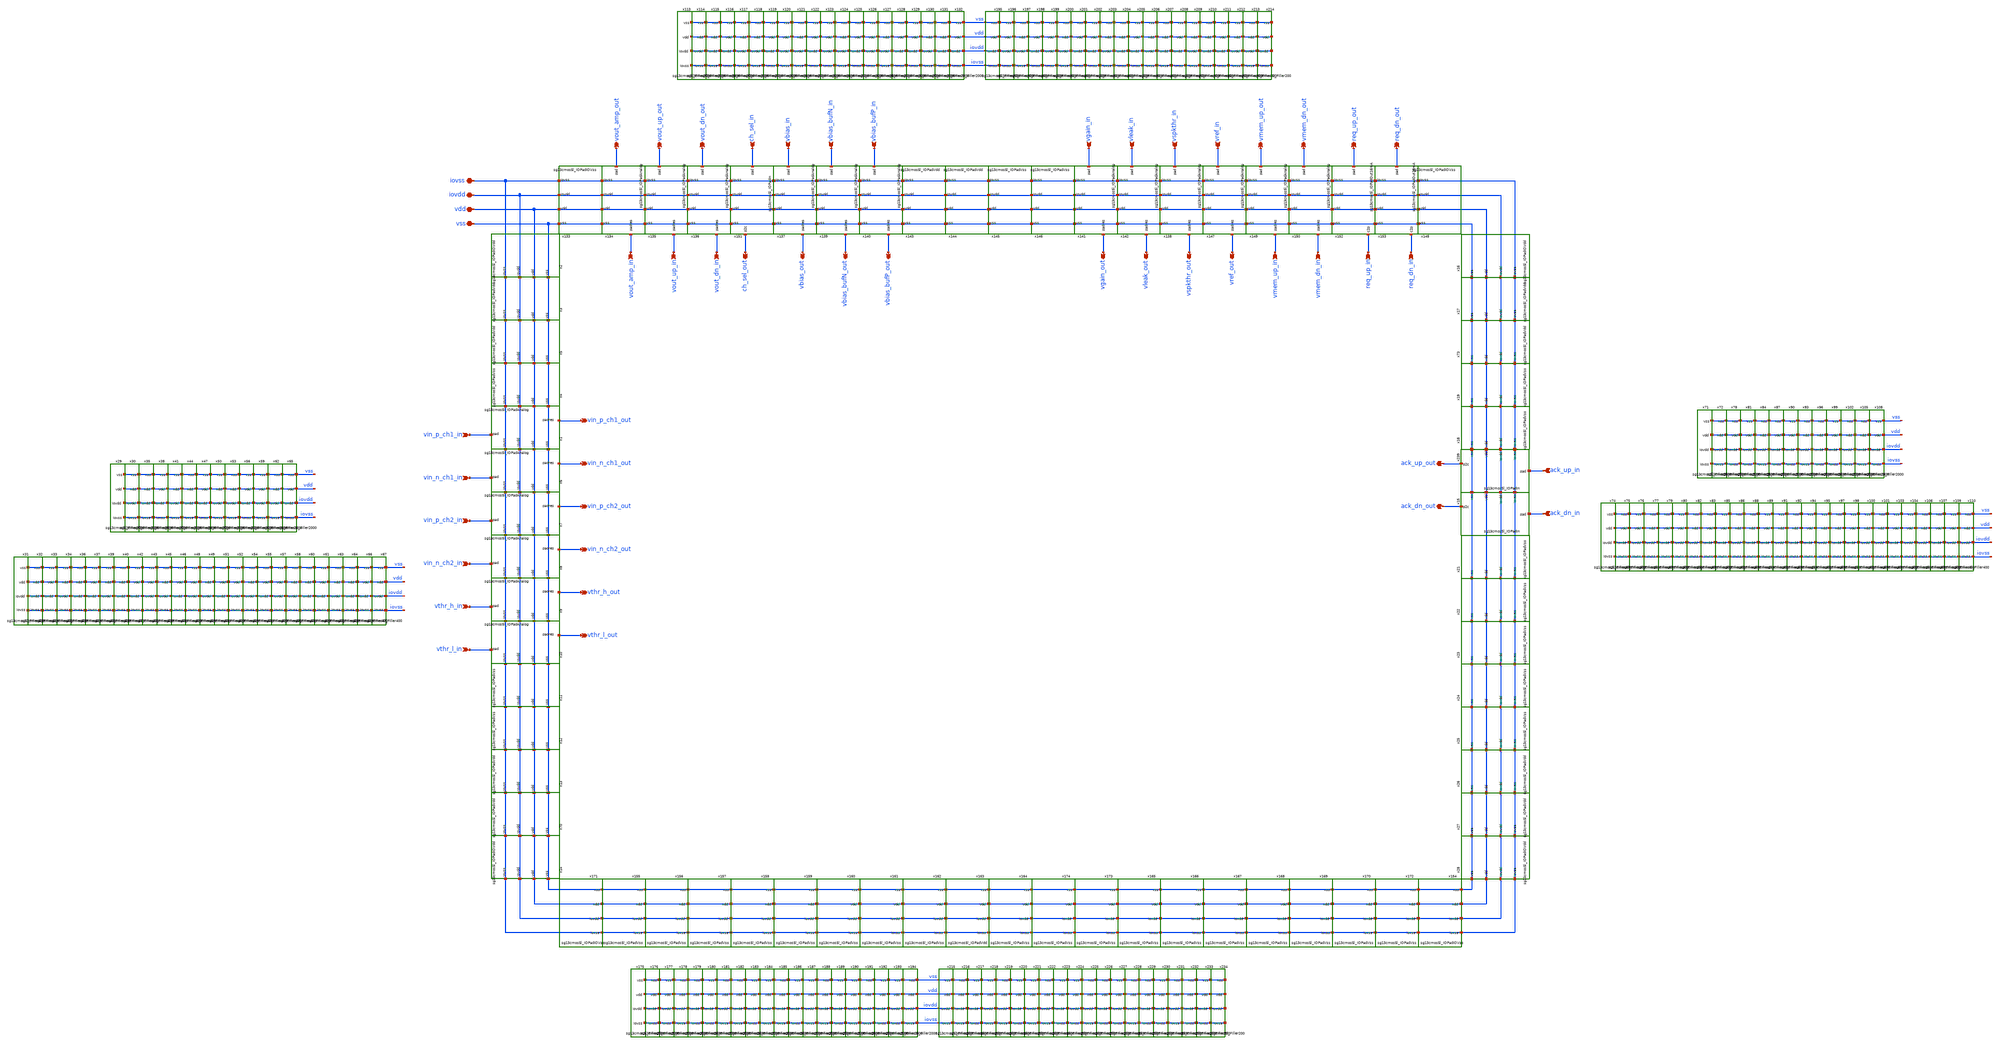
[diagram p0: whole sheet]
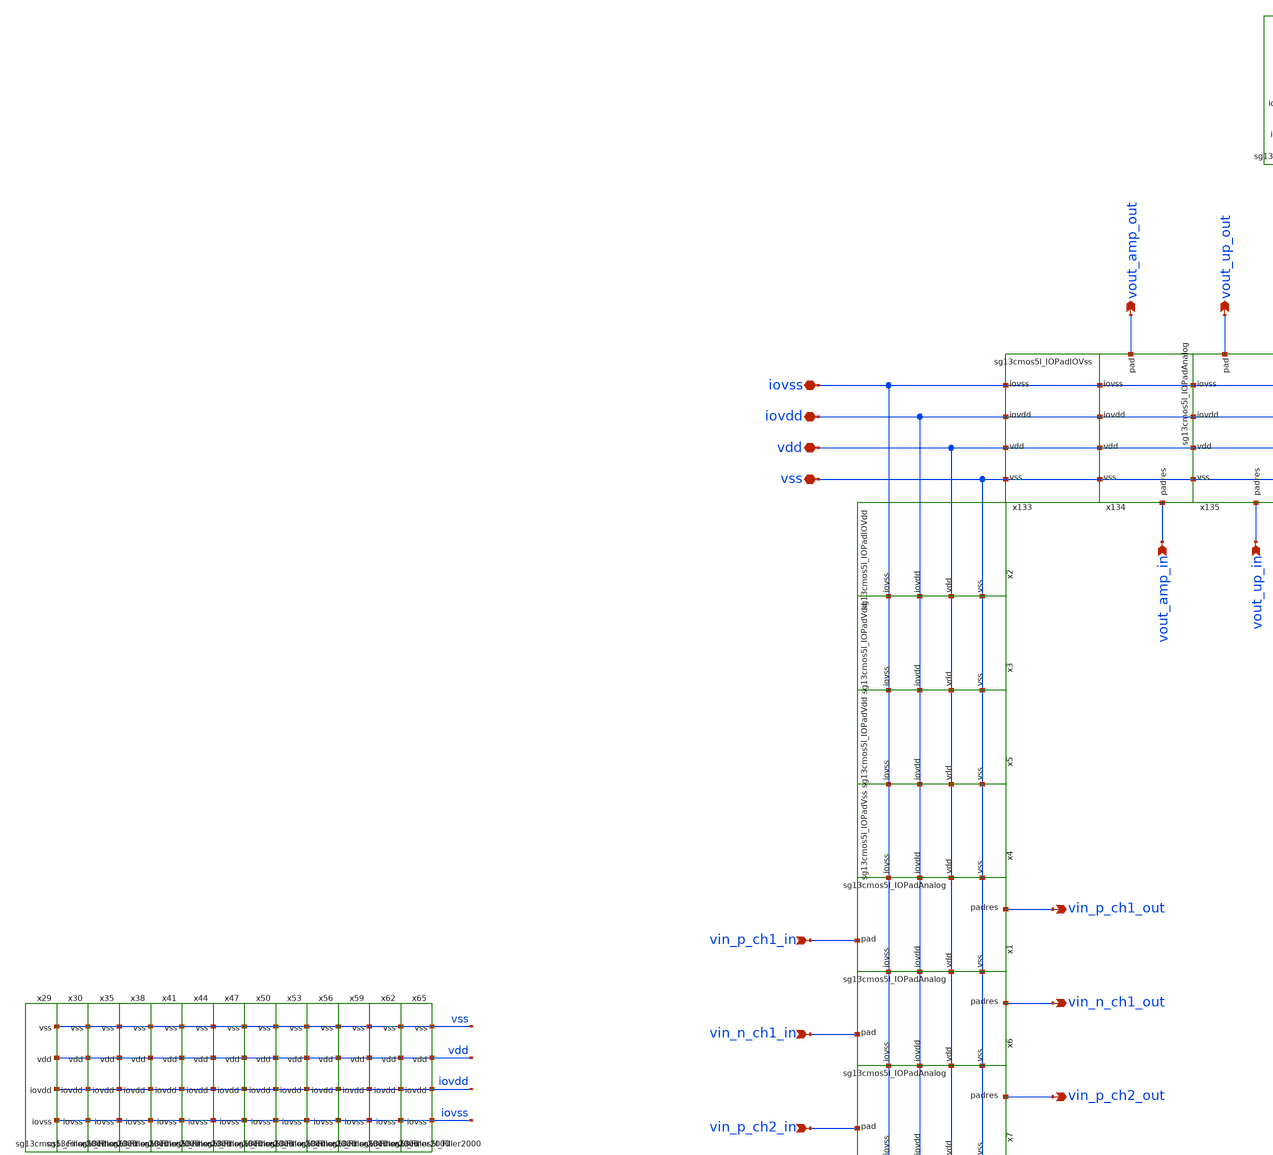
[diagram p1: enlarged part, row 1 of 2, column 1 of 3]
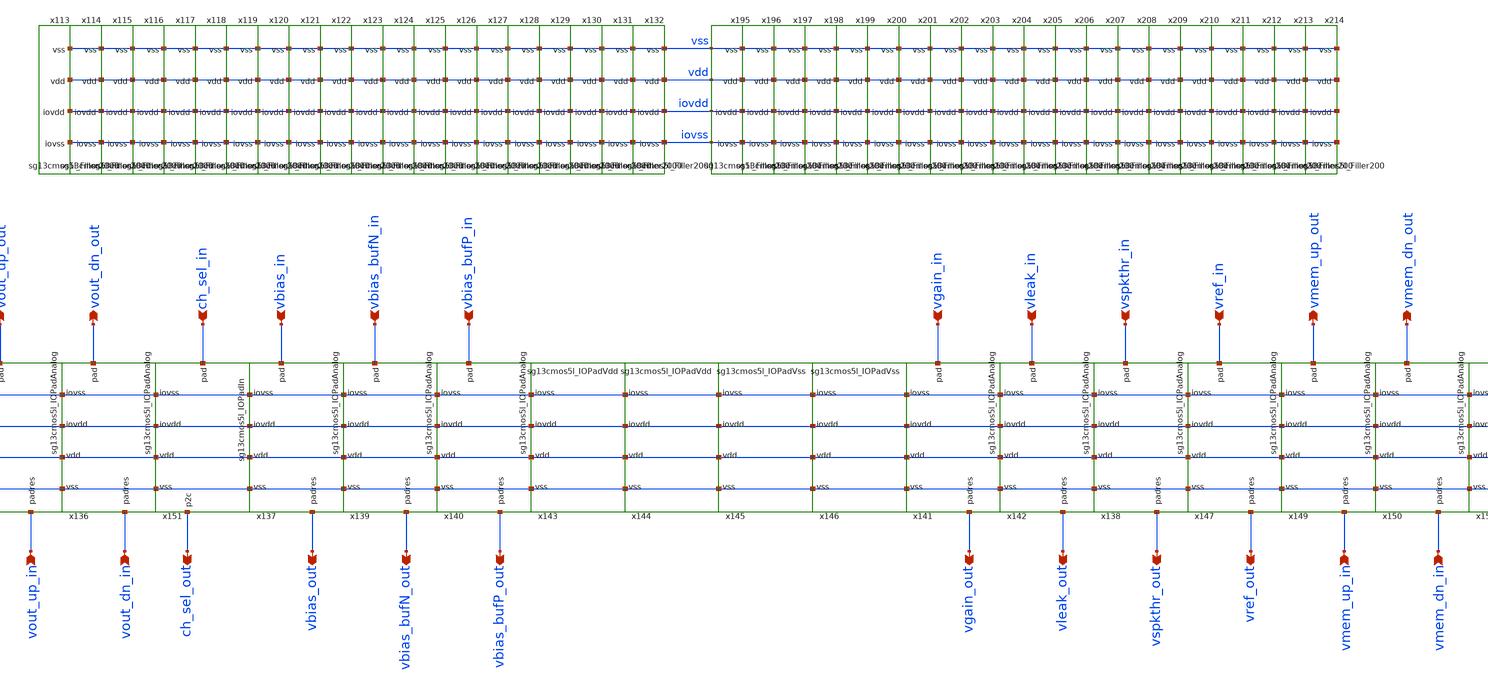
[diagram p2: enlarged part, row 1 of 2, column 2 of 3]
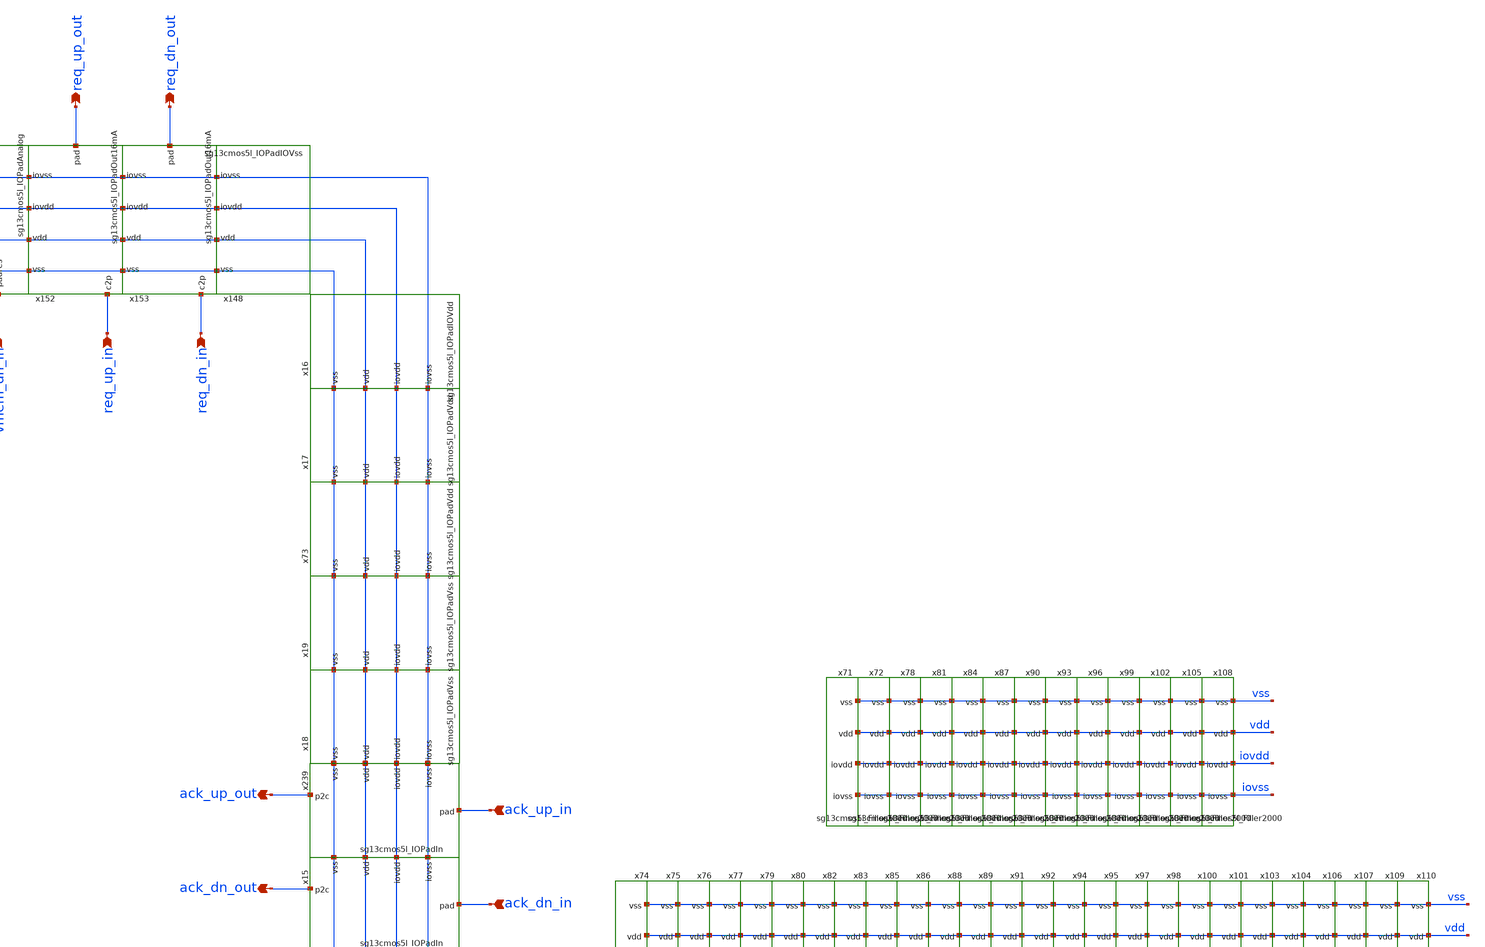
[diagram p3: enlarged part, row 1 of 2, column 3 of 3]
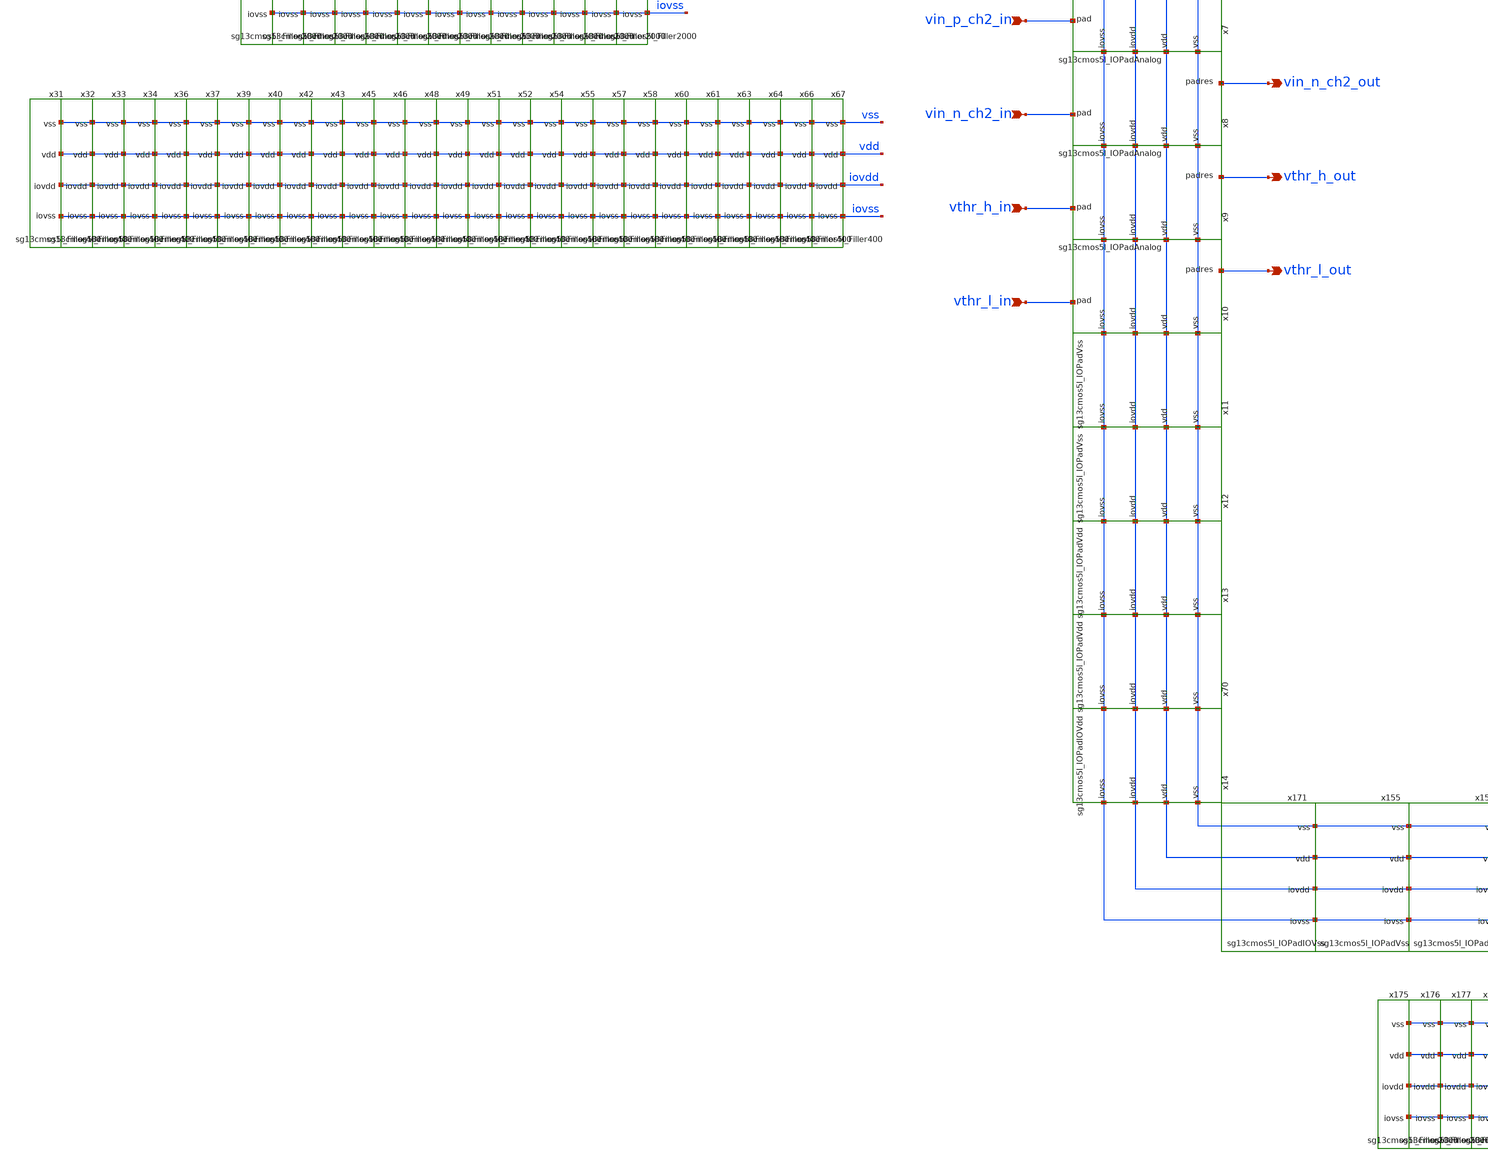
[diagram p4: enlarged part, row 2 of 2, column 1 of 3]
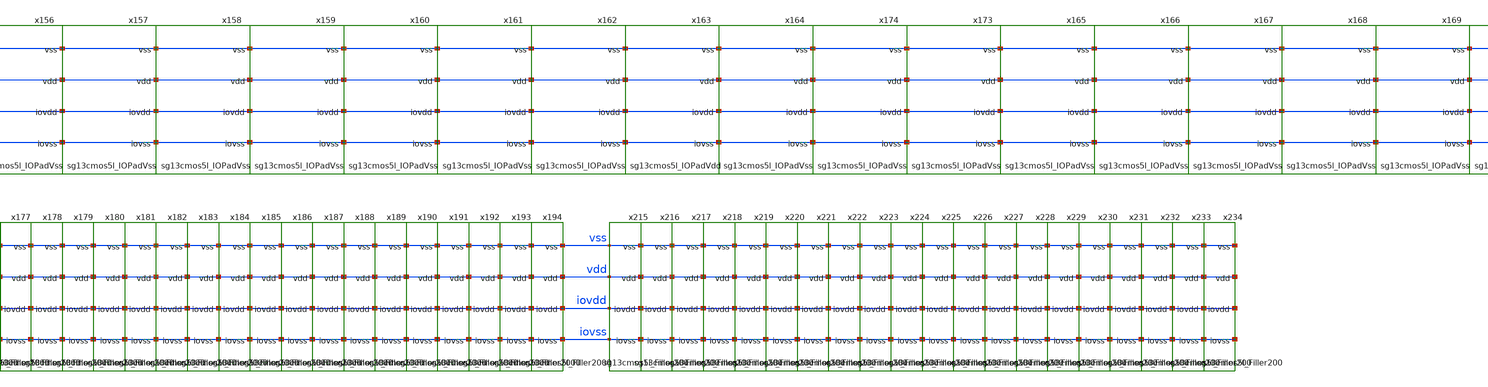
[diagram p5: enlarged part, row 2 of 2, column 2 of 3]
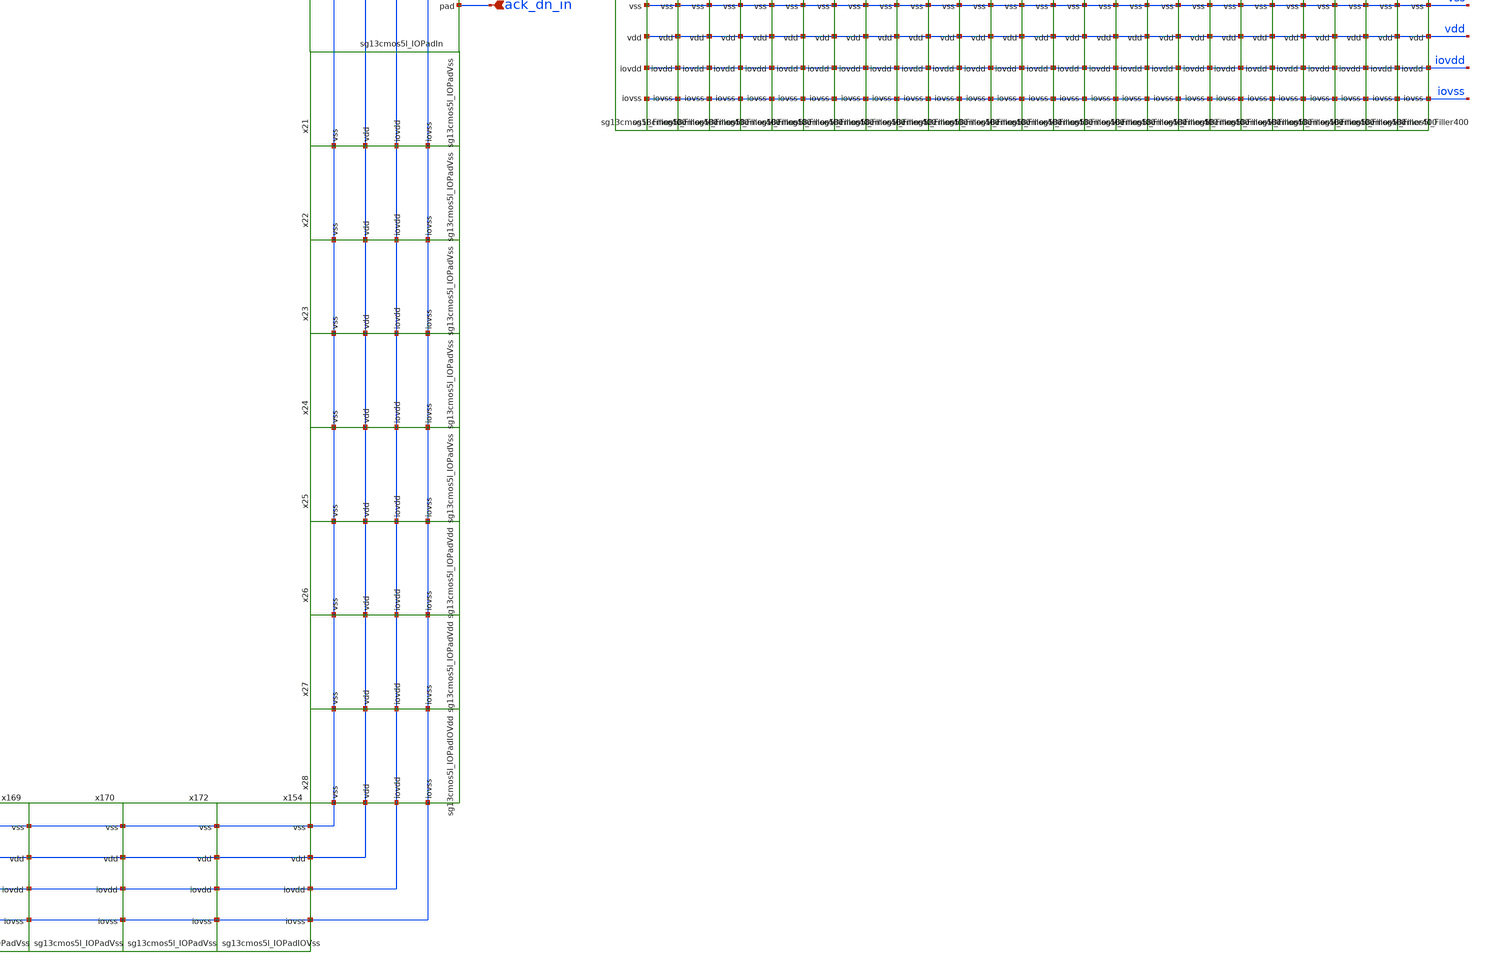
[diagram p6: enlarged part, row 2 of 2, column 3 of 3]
** sch_path: v2_feature_extr/padframe_old.sch
**.subckt padframe_old iovss iovdd vdd vss vin_p_ch1_in vin_n_ch1_in vin_p_ch2_in vin_n_ch2_in
*+ vin_p_ch1_out vin_n_ch1_out vin_p_ch2_out vin_n_ch2_out vthr_h_in vthr_l_in vthr_h_out vthr_l_out vout_amp_in
*+ vout_up_in vout_dn_in vout_amp_out vout_up_out vout_dn_out ch_sel_in ch_sel_out vbias_in vbias_out
*+ vbias_bufN_in vbias_bufN_out vbias_bufP_in vbias_bufP_out vgain_in vleak_in vspkthr_in vref_in vgain_out
*+ vleak_out vspkthr_out vref_out vmem_up_in vmem_dn_in req_up_in req_dn_in vmem_up_out vmem_dn_out req_up_out
*+ req_dn_out ack_up_in ack_up_out ack_dn_in ack_dn_out
*.iopin iovss
*.iopin iovdd
*.iopin vdd
*.iopin vss
*.ipin vin_p_ch1_in
*.ipin vin_n_ch1_in
*.ipin vin_p_ch2_in
*.ipin vin_n_ch2_in
*.opin vin_p_ch1_out
*.opin vin_n_ch1_out
*.opin vin_p_ch2_out
*.opin vin_n_ch2_out
*.ipin vthr_h_in
*.ipin vthr_l_in
*.opin vthr_h_out
*.opin vthr_l_out
*.ipin vout_amp_in
*.ipin vout_up_in
*.ipin vout_dn_in
*.opin vout_amp_out
*.opin vout_up_out
*.opin vout_dn_out
*.ipin ch_sel_in
*.opin ch_sel_out
*.ipin vbias_in
*.opin vbias_out
*.ipin vbias_bufN_in
*.opin vbias_bufN_out
*.ipin vbias_bufP_in
*.opin vbias_bufP_out
*.ipin vgain_in
*.ipin vleak_in
*.ipin vspkthr_in
*.ipin vref_in
*.opin vgain_out
*.opin vleak_out
*.opin vspkthr_out
*.opin vref_out
*.ipin vmem_up_in
*.ipin vmem_dn_in
*.ipin req_up_in
*.ipin req_dn_in
*.opin vmem_up_out
*.opin vmem_dn_out
*.opin req_up_out
*.opin req_dn_out
*.ipin ack_up_in
*.opin ack_up_out
*.ipin ack_dn_in
*.opin ack_dn_out
x1 iovdd iovss vin_p_ch1_in vin_p_ch1_out vdd vss sg13cmos5l_IOPadAnalog
x2 iovdd iovss vdd vss sg13cmos5l_IOPadIOVdd
x3 iovdd iovss vdd vss sg13cmos5l_IOPadVdd
x4 iovdd iovss vdd vss sg13cmos5l_IOPadVss
x5 iovdd iovss vdd vss sg13cmos5l_IOPadVdd
x6 iovdd iovss vin_n_ch1_in vin_n_ch1_out vdd vss sg13cmos5l_IOPadAnalog
x7 iovdd iovss vin_p_ch2_in vin_p_ch2_out vdd vss sg13cmos5l_IOPadAnalog
x8 iovdd iovss vin_n_ch2_in vin_n_ch2_out vdd vss sg13cmos5l_IOPadAnalog
x9 iovdd iovss vthr_h_in vthr_h_out vdd vss sg13cmos5l_IOPadAnalog
x10 iovdd iovss vthr_l_in vthr_l_out vdd vss sg13cmos5l_IOPadAnalog
x11 iovdd iovss vdd vss sg13cmos5l_IOPadVss
x12 iovdd iovss vdd vss sg13cmos5l_IOPadVss
x13 iovdd iovss vdd vss sg13cmos5l_IOPadVdd
x14 iovdd iovss vdd vss sg13cmos5l_IOPadIOVdd
x16 iovdd iovss vdd vss sg13cmos5l_IOPadIOVdd
x17 iovdd iovss vdd vss sg13cmos5l_IOPadVdd
x18 iovdd iovss vdd vss sg13cmos5l_IOPadVss
x19 iovdd iovss vdd vss sg13cmos5l_IOPadVss
x25 iovdd iovss vdd vss sg13cmos5l_IOPadVss
x26 iovdd iovss vdd vss sg13cmos5l_IOPadVdd
x27 iovdd iovss vdd vss sg13cmos5l_IOPadVdd
x28 iovdd iovss vdd vss sg13cmos5l_IOPadIOVdd
x21 iovdd iovss vdd vss sg13cmos5l_IOPadVss
x22 iovdd iovss vdd vss sg13cmos5l_IOPadVss
x23 iovdd iovss vdd vss sg13cmos5l_IOPadVss
x24 iovdd iovss vdd vss sg13cmos5l_IOPadVss
x29 iovdd iovss vdd vss sg13cmos5l_Filler2000
x30 iovdd iovss vdd vss sg13cmos5l_Filler2000
x31 iovdd iovss vdd vss sg13cmos5l_Filler400
x32 iovdd iovss vdd vss sg13cmos5l_Filler400
x33 iovdd iovss vdd vss sg13cmos5l_Filler400
x34 iovdd iovss vdd vss sg13cmos5l_Filler400
x35 iovdd iovss vdd vss sg13cmos5l_Filler2000
x36 iovdd iovss vdd vss sg13cmos5l_Filler400
x37 iovdd iovss vdd vss sg13cmos5l_Filler400
x38 iovdd iovss vdd vss sg13cmos5l_Filler2000
x39 iovdd iovss vdd vss sg13cmos5l_Filler400
x40 iovdd iovss vdd vss sg13cmos5l_Filler400
x41 iovdd iovss vdd vss sg13cmos5l_Filler2000
x42 iovdd iovss vdd vss sg13cmos5l_Filler400
x43 iovdd iovss vdd vss sg13cmos5l_Filler400
x44 iovdd iovss vdd vss sg13cmos5l_Filler2000
x45 iovdd iovss vdd vss sg13cmos5l_Filler400
x46 iovdd iovss vdd vss sg13cmos5l_Filler400
x47 iovdd iovss vdd vss sg13cmos5l_Filler2000
x48 iovdd iovss vdd vss sg13cmos5l_Filler400
x49 iovdd iovss vdd vss sg13cmos5l_Filler400
x50 iovdd iovss vdd vss sg13cmos5l_Filler2000
x51 iovdd iovss vdd vss sg13cmos5l_Filler400
x52 iovdd iovss vdd vss sg13cmos5l_Filler400
x53 iovdd iovss vdd vss sg13cmos5l_Filler2000
x54 iovdd iovss vdd vss sg13cmos5l_Filler400
x55 iovdd iovss vdd vss sg13cmos5l_Filler400
x56 iovdd iovss vdd vss sg13cmos5l_Filler2000
x57 iovdd iovss vdd vss sg13cmos5l_Filler400
x58 iovdd iovss vdd vss sg13cmos5l_Filler400
x59 iovdd iovss vdd vss sg13cmos5l_Filler2000
x60 iovdd iovss vdd vss sg13cmos5l_Filler400
x61 iovdd iovss vdd vss sg13cmos5l_Filler400
x62 iovdd iovss vdd vss sg13cmos5l_Filler2000
x63 iovdd iovss vdd vss sg13cmos5l_Filler400
x64 iovdd iovss vdd vss sg13cmos5l_Filler400
x65 iovdd iovss vdd vss sg13cmos5l_Filler2000
x66 iovdd iovss vdd vss sg13cmos5l_Filler400
x67 iovdd iovss vdd vss sg13cmos5l_Filler400
x70 iovdd iovss vdd vss sg13cmos5l_IOPadVdd
x73 iovdd iovss vdd vss sg13cmos5l_IOPadVdd
x113 iovdd iovss vdd vss sg13cmos5l_Filler2000
x114 iovdd iovss vdd vss sg13cmos5l_Filler2000
x115 iovdd iovss vdd vss sg13cmos5l_Filler2000
x116 iovdd iovss vdd vss sg13cmos5l_Filler2000
x117 iovdd iovss vdd vss sg13cmos5l_Filler2000
x118 iovdd iovss vdd vss sg13cmos5l_Filler2000
x119 iovdd iovss vdd vss sg13cmos5l_Filler2000
x120 iovdd iovss vdd vss sg13cmos5l_Filler2000
x121 iovdd iovss vdd vss sg13cmos5l_Filler2000
x122 iovdd iovss vdd vss sg13cmos5l_Filler2000
x123 iovdd iovss vdd vss sg13cmos5l_Filler2000
x124 iovdd iovss vdd vss sg13cmos5l_Filler2000
x125 iovdd iovss vdd vss sg13cmos5l_Filler2000
x126 iovdd iovss vdd vss sg13cmos5l_Filler2000
x127 iovdd iovss vdd vss sg13cmos5l_Filler2000
x128 iovdd iovss vdd vss sg13cmos5l_Filler2000
x129 iovdd iovss vdd vss sg13cmos5l_Filler2000
x130 iovdd iovss vdd vss sg13cmos5l_Filler2000
x131 iovdd iovss vdd vss sg13cmos5l_Filler2000
x132 iovdd iovss vdd vss sg13cmos5l_Filler2000
x133 iovdd iovss vdd vss sg13cmos5l_IOPadIOVss
x134 iovdd iovss vout_amp_out vout_amp_in vdd vss sg13cmos5l_IOPadAnalog
x135 iovdd iovss vout_up_out vout_up_in vdd vss sg13cmos5l_IOPadAnalog
x136 iovdd iovss vout_dn_out vout_dn_in vdd vss sg13cmos5l_IOPadAnalog
x139 iovdd iovss vbias_bufN_in vbias_bufN_out vdd vss sg13cmos5l_IOPadAnalog
x140 iovdd iovss vbias_bufP_in vbias_bufP_out vdd vss sg13cmos5l_IOPadAnalog
x141 iovdd iovss vgain_in vgain_out vdd vss sg13cmos5l_IOPadAnalog
x142 iovdd iovss vleak_in vleak_out vdd vss sg13cmos5l_IOPadAnalog
x149 iovdd iovss vmem_up_out vmem_up_in vdd vss sg13cmos5l_IOPadAnalog
x150 iovdd iovss vmem_dn_out vmem_dn_in vdd vss sg13cmos5l_IOPadAnalog
x137 iovdd iovss vbias_in vbias_out vdd vss sg13cmos5l_IOPadAnalog
x138 iovdd iovss vspkthr_in vspkthr_out vdd vss sg13cmos5l_IOPadAnalog
x143 iovdd iovss vdd vss sg13cmos5l_IOPadVdd
x144 iovdd iovss vdd vss sg13cmos5l_IOPadVdd
x145 iovdd iovss vdd vss sg13cmos5l_IOPadVss
x146 iovdd iovss vdd vss sg13cmos5l_IOPadVss
x147 iovdd iovss vref_in vref_out vdd vss sg13cmos5l_IOPadAnalog
x148 iovdd iovss vdd vss sg13cmos5l_IOPadIOVss
x152 req_up_in iovdd iovss req_up_out vdd vss sg13cmos5l_IOPadOut16mA
x153 req_dn_in iovdd iovss req_dn_out vdd vss sg13cmos5l_IOPadOut16mA
x154 iovdd iovss vdd vss sg13cmos5l_IOPadIOVss
x171 iovdd iovss vdd vss sg13cmos5l_IOPadIOVss
x155 iovdd iovss vdd vss sg13cmos5l_IOPadVss
x156 iovdd iovss vdd vss sg13cmos5l_IOPadVss
x157 iovdd iovss vdd vss sg13cmos5l_IOPadVss
x158 iovdd iovss vdd vss sg13cmos5l_IOPadVss
x159 iovdd iovss vdd vss sg13cmos5l_IOPadVss
x160 iovdd iovss vdd vss sg13cmos5l_IOPadVss
x161 iovdd iovss vdd vss sg13cmos5l_IOPadVss
x162 iovdd iovss vdd vss sg13cmos5l_IOPadVss
x163 iovdd iovss vdd vss sg13cmos5l_IOPadVdd
x164 iovdd iovss vdd vss sg13cmos5l_IOPadVss
x165 iovdd iovss vdd vss sg13cmos5l_IOPadVss
x166 iovdd iovss vdd vss sg13cmos5l_IOPadVss
x167 iovdd iovss vdd vss sg13cmos5l_IOPadVss
x168 iovdd iovss vdd vss sg13cmos5l_IOPadVss
x169 iovdd iovss vdd vss sg13cmos5l_IOPadVss
x170 iovdd iovss vdd vss sg13cmos5l_IOPadVss
x172 iovdd iovss vdd vss sg13cmos5l_IOPadVss
x173 iovdd iovss vdd vss sg13cmos5l_IOPadVss
x174 iovdd iovss vdd vss sg13cmos5l_IOPadVss
x71 iovdd iovss vdd vss sg13cmos5l_Filler2000
x72 iovdd iovss vdd vss sg13cmos5l_Filler2000
x74 iovdd iovss vdd vss sg13cmos5l_Filler400
x75 iovdd iovss vdd vss sg13cmos5l_Filler400
x76 iovdd iovss vdd vss sg13cmos5l_Filler400
x77 iovdd iovss vdd vss sg13cmos5l_Filler400
x78 iovdd iovss vdd vss sg13cmos5l_Filler2000
x79 iovdd iovss vdd vss sg13cmos5l_Filler400
x80 iovdd iovss vdd vss sg13cmos5l_Filler400
x81 iovdd iovss vdd vss sg13cmos5l_Filler2000
x82 iovdd iovss vdd vss sg13cmos5l_Filler400
x83 iovdd iovss vdd vss sg13cmos5l_Filler400
x84 iovdd iovss vdd vss sg13cmos5l_Filler2000
x85 iovdd iovss vdd vss sg13cmos5l_Filler400
x86 iovdd iovss vdd vss sg13cmos5l_Filler400
x87 iovdd iovss vdd vss sg13cmos5l_Filler2000
x88 iovdd iovss vdd vss sg13cmos5l_Filler400
x89 iovdd iovss vdd vss sg13cmos5l_Filler400
x90 iovdd iovss vdd vss sg13cmos5l_Filler2000
x91 iovdd iovss vdd vss sg13cmos5l_Filler400
x92 iovdd iovss vdd vss sg13cmos5l_Filler400
x93 iovdd iovss vdd vss sg13cmos5l_Filler2000
x94 iovdd iovss vdd vss sg13cmos5l_Filler400
x95 iovdd iovss vdd vss sg13cmos5l_Filler400
x96 iovdd iovss vdd vss sg13cmos5l_Filler2000
x97 iovdd iovss vdd vss sg13cmos5l_Filler400
x98 iovdd iovss vdd vss sg13cmos5l_Filler400
x99 iovdd iovss vdd vss sg13cmos5l_Filler2000
x100 iovdd iovss vdd vss sg13cmos5l_Filler400
x101 iovdd iovss vdd vss sg13cmos5l_Filler400
x102 iovdd iovss vdd vss sg13cmos5l_Filler2000
x103 iovdd iovss vdd vss sg13cmos5l_Filler400
x104 iovdd iovss vdd vss sg13cmos5l_Filler400
x105 iovdd iovss vdd vss sg13cmos5l_Filler2000
x106 iovdd iovss vdd vss sg13cmos5l_Filler400
x107 iovdd iovss vdd vss sg13cmos5l_Filler400
x108 iovdd iovss vdd vss sg13cmos5l_Filler2000
x109 iovdd iovss vdd vss sg13cmos5l_Filler400
x110 iovdd iovss vdd vss sg13cmos5l_Filler400
x175 iovdd iovss vdd vss sg13cmos5l_Filler2000
x176 iovdd iovss vdd vss sg13cmos5l_Filler2000
x177 iovdd iovss vdd vss sg13cmos5l_Filler2000
x178 iovdd iovss vdd vss sg13cmos5l_Filler2000
x179 iovdd iovss vdd vss sg13cmos5l_Filler2000
x180 iovdd iovss vdd vss sg13cmos5l_Filler2000
x181 iovdd iovss vdd vss sg13cmos5l_Filler2000
x182 iovdd iovss vdd vss sg13cmos5l_Filler2000
x183 iovdd iovss vdd vss sg13cmos5l_Filler2000
x184 iovdd iovss vdd vss sg13cmos5l_Filler2000
x185 iovdd iovss vdd vss sg13cmos5l_Filler2000
x186 iovdd iovss vdd vss sg13cmos5l_Filler2000
x187 iovdd iovss vdd vss sg13cmos5l_Filler2000
x188 iovdd iovss vdd vss sg13cmos5l_Filler2000
x189 iovdd iovss vdd vss sg13cmos5l_Filler2000
x190 iovdd iovss vdd vss sg13cmos5l_Filler2000
x191 iovdd iovss vdd vss sg13cmos5l_Filler2000
x192 iovdd iovss vdd vss sg13cmos5l_Filler2000
x193 iovdd iovss vdd vss sg13cmos5l_Filler2000
x194 iovdd iovss vdd vss sg13cmos5l_Filler2000
x195 iovdd iovss vdd vss sg13cmos5l_Filler200
x196 iovdd iovss vdd vss sg13cmos5l_Filler200
x197 iovdd iovss vdd vss sg13cmos5l_Filler200
x198 iovdd iovss vdd vss sg13cmos5l_Filler200
x199 iovdd iovss vdd vss sg13cmos5l_Filler200
x200 iovdd iovss vdd vss sg13cmos5l_Filler200
x201 iovdd iovss vdd vss sg13cmos5l_Filler200
x202 iovdd iovss vdd vss sg13cmos5l_Filler200
x203 iovdd iovss vdd vss sg13cmos5l_Filler200
x204 iovdd iovss vdd vss sg13cmos5l_Filler200
x205 iovdd iovss vdd vss sg13cmos5l_Filler200
x206 iovdd iovss vdd vss sg13cmos5l_Filler200
x207 iovdd iovss vdd vss sg13cmos5l_Filler200
x208 iovdd iovss vdd vss sg13cmos5l_Filler200
x209 iovdd iovss vdd vss sg13cmos5l_Filler200
x210 iovdd iovss vdd vss sg13cmos5l_Filler200
x211 iovdd iovss vdd vss sg13cmos5l_Filler200
x212 iovdd iovss vdd vss sg13cmos5l_Filler200
x213 iovdd iovss vdd vss sg13cmos5l_Filler200
x214 iovdd iovss vdd vss sg13cmos5l_Filler200
x215 iovdd iovss vdd vss sg13cmos5l_Filler200
x216 iovdd iovss vdd vss sg13cmos5l_Filler200
x217 iovdd iovss vdd vss sg13cmos5l_Filler200
x218 iovdd iovss vdd vss sg13cmos5l_Filler200
x219 iovdd iovss vdd vss sg13cmos5l_Filler200
x220 iovdd iovss vdd vss sg13cmos5l_Filler200
x221 iovdd iovss vdd vss sg13cmos5l_Filler200
x222 iovdd iovss vdd vss sg13cmos5l_Filler200
x223 iovdd iovss vdd vss sg13cmos5l_Filler200
x224 iovdd iovss vdd vss sg13cmos5l_Filler200
x225 iovdd iovss vdd vss sg13cmos5l_Filler200
x226 iovdd iovss vdd vss sg13cmos5l_Filler200
x227 iovdd iovss vdd vss sg13cmos5l_Filler200
x228 iovdd iovss vdd vss sg13cmos5l_Filler200
x229 iovdd iovss vdd vss sg13cmos5l_Filler200
x230 iovdd iovss vdd vss sg13cmos5l_Filler200
x231 iovdd iovss vdd vss sg13cmos5l_Filler200
x232 iovdd iovss vdd vss sg13cmos5l_Filler200
x233 iovdd iovss vdd vss sg13cmos5l_Filler200
x234 iovdd iovss vdd vss sg13cmos5l_Filler200
x151 iovdd iovss ch_sel_out ch_sel_in vdd vss sg13cmos5l_IOPadIn
x239 iovdd iovss ack_up_out ack_up_in vdd vss sg13cmos5l_IOPadIn
x15 iovdd iovss ack_dn_out ack_dn_in vdd vss sg13cmos5l_IOPadIn
**.ends

* expanding   symbol:  sg13cmos5l_IOPadAnalog.sym # of pins=6
** sym_path: v2_feature_extr/sg13cmos5l_IOPadAnalog.sym
.include /foss/pdks/ihp-sg13cmos5l/libs.ref/sg13cmos5l_io/cdl/sg13cmos5l_io.cdl

* expanding   symbol:  sg13cmos5l_IOPadIOVdd.sym # of pins=4
** sym_path: v2_feature_extr_withf/sg13cmos5l_IOPadIOVdd.sym
.include /foss/pdks/ihp-sg13cmos5l/libs.ref/sg13cmos5l_io/cdl/sg13cmos5l_io.cdl

* expanding   symbol:  sg13cmos5l_IOPadVdd.sym # of pins=4
** sym_path: v2_feature_extr/sg13cmos5l_IOPadVdd.sym
.include /foss/pdks/ihp-sg13cmos5l/libs.ref/sg13cmos5l_io/cdl/sg13cmos5l_io.cdl

* expanding   symbol:  sg13cmos5l_IOPadVss.sym # of pins=4
** sym_path: v2_feature_extr/sg13cmos5l_IOPadVss.sym
.include /foss/pdks/ihp-sg13cmos5l/libs.ref/sg13cmos5l_io/cdl/sg13cmos5l_io.cdl

* expanding   symbol:  sg13cmos5l_Filler2000.sym # of pins=4
** sym_path: v2_feature_extr/sg13cmos5l_Filler2000.sym
.include /foss/pdks/ihp-sg13cmos5l/libs.ref/sg13cmos5l_io/cdl/sg13cmos5l_io.cdl

* expanding   symbol:  sg13cmos5l_Filler400.sym # of pins=4
** sym_path: v2_feature_extr_withf/sg13cmos5l_Filler400.sym
.include /foss/pdks/ihp-sg13cmos5l/libs.ref/sg13cmos5l_io/cdl/sg13cmos5l_io.cdl

* expanding   symbol:  sg13cmos5l_IOPadIOVss.sym # of pins=4
** sym_path: v2_feature_extr/sg13cmos5l_IOPadIOVss.sym
.include /foss/pdks/ihp-sg13cmos5l/libs.ref/sg13cmos5l_io/cdl/sg13cmos5l_io.cdl

* expanding   symbol:  sg13cmos5l_IOPadOut16mA.sym # of pins=6
** sym_path: v2_feature_extr/sg13cmos5l_IOPadOut16mA.sym
.include /foss/pdks/ihp-sg13cmos5l/libs.ref/sg13cmos5l_io/cdl/sg13cmos5l_io.cdl

* expanding   symbol:  sg13cmos5l_Filler200.sym # of pins=4
** sym_path: v2_feature_extr/sg13cmos5l_Filler200.sym
.include /foss/pdks/ihp-sg13cmos5l/libs.ref/sg13cmos5l_io/cdl/sg13cmos5l_io.cdl

* expanding   symbol:  sg13cmos5l_IOPadIn.sym # of pins=6
** sym_path: v2_feature_extr/sg13cmos5l_IOPadIn.sym
.include /foss/pdks/ihp-sg13cmos5l/libs.ref/sg13cmos5l_io/cdl/sg13cmos5l_io.cdl
.end
